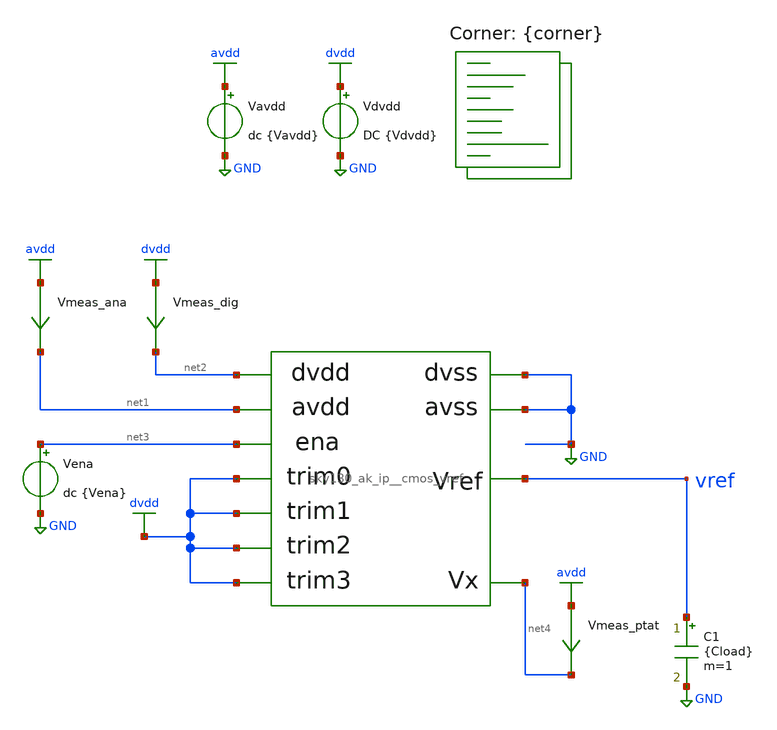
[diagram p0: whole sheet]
** sch_path: cace/tb_power.sch
**.subckt tb_power
Vavdd avdd GND dc {Vavdd}
X1 net1 GND dvdd vref net4 dvdd dvdd dvdd net2 GND net3 sky130_ak_ip__cmos_vref
Vdvdd dvdd GND DC {Vdvdd}
C1 vref GND {Cload} m=1
Vena net3 GND dc {Vena}
Vmeas_ana avdd net1 0
.save i(vmeas_ana)
Vmeas_dig dvdd net2 0
.save i(vmeas_dig)
Vmeas_ptat avdd net4 0
.save i(vmeas_ptat)
**** begin user architecture code


.option TEMP={temperature}
.option warn=1
.option savecurrents
.control
save all
op
print I(Vmeas_ana), I(vmeas_dig), I(Vavdd)
let total_current = I(Vmeas_ana) + I(vmeas_dig)
set wr_singlescale
wrdata {simpath}/{filename}_{N}.data -I(Vavdd)
quit
.endc


.lib $::SKYWATER_MODELS/sky130.lib.spice {corner}
**** end user architecture code
**.ends

* expanding   symbol:  ../xschem/sky130_ak_ip__cmos_vref.sym # of pins=11
** sym_path: xschem/sky130_ak_ip__cmos_vref.sym
** sch_path: xschem/sky130_ak_ip__cmos_vref.sch
.subckt sky130_ak_ip__cmos_vref avdd avss trim0 vref vx trim1 trim2 trim3 dvdd dvss ena
*.opin vref
*.iopin avss
*.iopin avdd
*.opin vx
*.ipin trim0
*.ipin trim1
*.ipin trim2
*.ipin trim3
*.iopin dvdd
*.iopin dvss
*.iopin avdd
*.ipin ena
XM3 net1 net3 vx GND sky130_fd_pr__nfet_g5v0d10v5 L=1 W=100 nf=5 ad='int((nf+1)/2) * W/nf * 0.29' as='int((nf+2)/2) * W/nf * 0.29'
+ pd='2*int((nf+1)/2) * (W/nf + 0.29)' ps='2*int((nf+2)/2) * (W/nf + 0.29)' nrd='0.29 / W' nrs='0.29 / W'
+ sa=0 sb=0 sd=0 mult=1 m=1
XM4 net2 net3 avss GND sky130_fd_pr__nfet_g5v0d10v5 L=1 W=5 nf=1 ad='int((nf+1)/2) * W/nf * 0.29' as='int((nf+2)/2) * W/nf * 0.29'
+ pd='2*int((nf+1)/2) * (W/nf + 0.29)' ps='2*int((nf+2)/2) * (W/nf + 0.29)' nrd='0.29 / W' nrs='0.29 / W'
+ sa=0 sb=0 sd=0 mult=1 m=1
XM5 net4 vref net1 GND sky130_fd_pr__nfet_g5v0d10v5 L=10 W=10 nf=1 ad='int((nf+1)/2) * W/nf * 0.29' as='int((nf+2)/2) * W/nf * 0.29'
+ pd='2*int((nf+1)/2) * (W/nf + 0.29)' ps='2*int((nf+2)/2) * (W/nf + 0.29)' nrd='0.29 / W' nrs='0.29 / W'
+ sa=0 sb=0 sd=0 mult=1 m=1
XM6 net3 vref net2 GND sky130_fd_pr__nfet_g5v0d10v5 L=10 W=10 nf=1 ad='int((nf+1)/2) * W/nf * 0.29' as='int((nf+2)/2) * W/nf * 0.29'
+ pd='2*int((nf+1)/2) * (W/nf + 0.29)' ps='2*int((nf+2)/2) * (W/nf + 0.29)' nrd='0.29 / W' nrs='0.29 / W'
+ sa=0 sb=0 sd=0 mult=1 m=1
XM7 net4 net4 avdd_ena avdd sky130_fd_pr__pfet_g5v0d10v5 L=10 W=5 nf=1 ad='int((nf+1)/2) * W/nf * 0.29'
+ as='int((nf+2)/2) * W/nf * 0.29' pd='2*int((nf+1)/2) * (W/nf + 0.29)' ps='2*int((nf+2)/2) * (W/nf + 0.29)'
+ nrd='0.29 / W' nrs='0.29 / W' sa=0 sb=0 sd=0 mult=1 m=1
XM8 net3 net4 avdd_ena avdd sky130_fd_pr__pfet_g5v0d10v5 L=10 W=5 nf=1 ad='int((nf+1)/2) * W/nf * 0.29'
+ as='int((nf+2)/2) * W/nf * 0.29' pd='2*int((nf+1)/2) * (W/nf + 0.29)' ps='2*int((nf+2)/2) * (W/nf + 0.29)'
+ nrd='0.29 / W' nrs='0.29 / W' sa=0 sb=0 sd=0 mult=1 m=1
XM9 vref net4 avdd_ena avdd sky130_fd_pr__pfet_g5v0d10v5 L=10 W=50 nf=1 ad='int((nf+1)/2) * W/nf * 0.29'
+ as='int((nf+2)/2) * W/nf * 0.29' pd='2*int((nf+1)/2) * (W/nf + 0.29)' ps='2*int((nf+2)/2) * (W/nf + 0.29)'
+ nrd='0.29 / W' nrs='0.29 / W' sa=0 sb=0 sd=0 mult=1 m=1
XM10 net5 net3 avss GND sky130_fd_pr__nfet_g5v0d10v5 L=1 W=5 nf=1 ad='int((nf+1)/2) * W/nf * 0.29' as='int((nf+2)/2) * W/nf * 0.29'
+ pd='2*int((nf+1)/2) * (W/nf + 0.29)' ps='2*int((nf+2)/2) * (W/nf + 0.29)' nrd='0.29 / W' nrs='0.29 / W'
+ sa=0 sb=0 sd=0 mult=1 m=1
XM11 net4 net5 avss GND sky130_fd_pr__nfet_g5v0d10v5 L=1 W=5 nf=1 ad='int((nf+1)/2) * W/nf * 0.29' as='int((nf+2)/2) * W/nf * 0.29'
+ pd='2*int((nf+1)/2) * (W/nf + 0.29)' ps='2*int((nf+2)/2) * (W/nf + 0.29)' nrd='0.29 / W' nrs='0.29 / W'
+ sa=0 sb=0 sd=0 mult=1 m=1
XC1 avdd_ena net5 sky130_fd_pr__cap_mim_m3_1 W=5 L=5 MF=1 m=1
XM12 vref net4 net9 avdd sky130_fd_pr__pfet_g5v0d10v5 L=10 W=1 nf=1 ad='int((nf+1)/2) * W/nf * 0.29'
+ as='int((nf+2)/2) * W/nf * 0.29' pd='2*int((nf+1)/2) * (W/nf + 0.29)' ps='2*int((nf+2)/2) * (W/nf + 0.29)'
+ nrd='0.29 / W' nrs='0.29 / W' sa=0 sb=0 sd=0 mult=1 m=1
XM13 vref net4 net8 avdd sky130_fd_pr__pfet_g5v0d10v5 L=10 W=2 nf=1 ad='int((nf+1)/2) * W/nf * 0.29'
+ as='int((nf+2)/2) * W/nf * 0.29' pd='2*int((nf+1)/2) * (W/nf + 0.29)' ps='2*int((nf+2)/2) * (W/nf + 0.29)'
+ nrd='0.29 / W' nrs='0.29 / W' sa=0 sb=0 sd=0 mult=1 m=1
XM14 net9 trim0 avdd_ena dvdd sky130_fd_pr__pfet_g5v0d10v5 L=0.15 W=1 nf=1 ad='int((nf+1)/2) * W/nf * 0.29'
+ as='int((nf+2)/2) * W/nf * 0.29' pd='2*int((nf+1)/2) * (W/nf + 0.29)' ps='2*int((nf+2)/2) * (W/nf + 0.29)'
+ nrd='0.29 / W' nrs='0.29 / W' sa=0 sb=0 sd=0 mult=1 m=1
XM15 net8 trim1 avdd_ena dvdd sky130_fd_pr__pfet_g5v0d10v5 L=0.15 W=1 nf=1 ad='int((nf+1)/2) * W/nf * 0.29'
+ as='int((nf+2)/2) * W/nf * 0.29' pd='2*int((nf+1)/2) * (W/nf + 0.29)' ps='2*int((nf+2)/2) * (W/nf + 0.29)'
+ nrd='0.29 / W' nrs='0.29 / W' sa=0 sb=0 sd=0 mult=1 m=1
XM16 vref net4 net7 avdd sky130_fd_pr__pfet_g5v0d10v5 L=10 W=4 nf=1 ad='int((nf+1)/2) * W/nf * 0.29'
+ as='int((nf+2)/2) * W/nf * 0.29' pd='2*int((nf+1)/2) * (W/nf + 0.29)' ps='2*int((nf+2)/2) * (W/nf + 0.29)'
+ nrd='0.29 / W' nrs='0.29 / W' sa=0 sb=0 sd=0 mult=1 m=1
XM17 net7 trim2 avdd_ena dvdd sky130_fd_pr__pfet_g5v0d10v5 L=0.15 W=1 nf=1 ad='int((nf+1)/2) * W/nf * 0.29'
+ as='int((nf+2)/2) * W/nf * 0.29' pd='2*int((nf+1)/2) * (W/nf + 0.29)' ps='2*int((nf+2)/2) * (W/nf + 0.29)'
+ nrd='0.29 / W' nrs='0.29 / W' sa=0 sb=0 sd=0 mult=1 m=1
XM18 vref net4 net6 avdd sky130_fd_pr__pfet_g5v0d10v5 L=10 W=8 nf=1 ad='int((nf+1)/2) * W/nf * 0.29'
+ as='int((nf+2)/2) * W/nf * 0.29' pd='2*int((nf+1)/2) * (W/nf + 0.29)' ps='2*int((nf+2)/2) * (W/nf + 0.29)'
+ nrd='0.29 / W' nrs='0.29 / W' sa=0 sb=0 sd=0 mult=1 m=1
XM19 net6 trim3 avdd_ena dvdd sky130_fd_pr__pfet_g5v0d10v5 L=0.15 W=1 nf=1 ad='int((nf+1)/2) * W/nf * 0.29'
+ as='int((nf+2)/2) * W/nf * 0.29' pd='2*int((nf+1)/2) * (W/nf + 0.29)' ps='2*int((nf+2)/2) * (W/nf + 0.29)'
+ nrd='0.29 / W' nrs='0.29 / W' sa=0 sb=0 sd=0 mult=1 m=1
XM1 vx vref avss GND sky130_fd_pr__nfet_g5v0d10v5 L=10 W=2.5 nf=1 ad='int((nf+1)/2) * W/nf * 0.29' as='int((nf+2)/2) * W/nf * 0.29'
+ pd='2*int((nf+1)/2) * (W/nf + 0.29)' ps='2*int((nf+2)/2) * (W/nf + 0.29)' nrd='0.29 / W' nrs='0.29 / W'
+ sa=0 sb=0 sd=0 mult=1 m=1
XM2 vref vref vx GND sky130_fd_pr__nfet_g5v0d10v5 L=10 W=2 nf=1 ad='int((nf+1)/2) * W/nf * 0.29' as='int((nf+2)/2) * W/nf * 0.29'
+ pd='2*int((nf+1)/2) * (W/nf + 0.29)' ps='2*int((nf+2)/2) * (W/nf + 0.29)' nrd='0.29 / W' nrs='0.29 / W'
+ sa=0 sb=0 sd=0 mult=1 m=1
XM20 avdd_ena ena avdd dvdd sky130_fd_pr__pfet_g5v0d10v5 L=0.3 W=5 nf=1 ad='int((nf+1)/2) * W/nf * 0.29'
+ as='int((nf+2)/2) * W/nf * 0.29' pd='2*int((nf+1)/2) * (W/nf + 0.29)' ps='2*int((nf+2)/2) * (W/nf + 0.29)'
+ nrd='0.29 / W' nrs='0.29 / W' sa=0 sb=0 sd=0 mult=1 m=1
.ends

.GLOBAL avdd
.GLOBAL GND
.GLOBAL dvdd
.end
